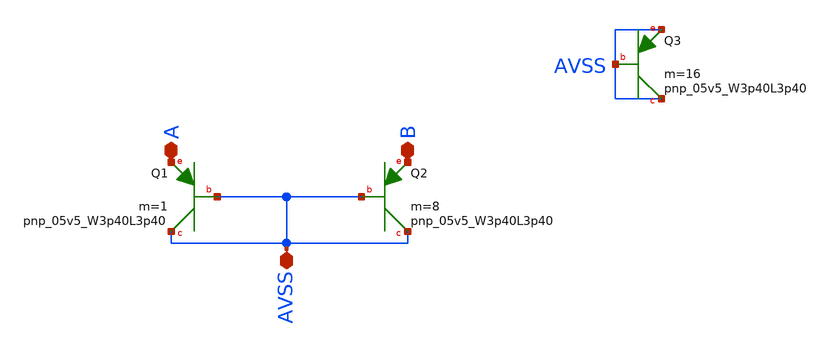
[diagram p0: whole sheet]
** sch_path: magic/bjt.sch
**.subckt bjt AVSS A B
*.iopin AVSS
*.iopin A
*.iopin B
XQ1 AVSS AVSS A sky130_fd_pr__pnp_05v5_W3p40L3p40 m=1
XQ2 AVSS AVSS B sky130_fd_pr__pnp_05v5_W3p40L3p40 m=8
XQ3 AVSS AVSS AVSS sky130_fd_pr__pnp_05v5_W3p40L3p40 m=16
**.ends
.end
